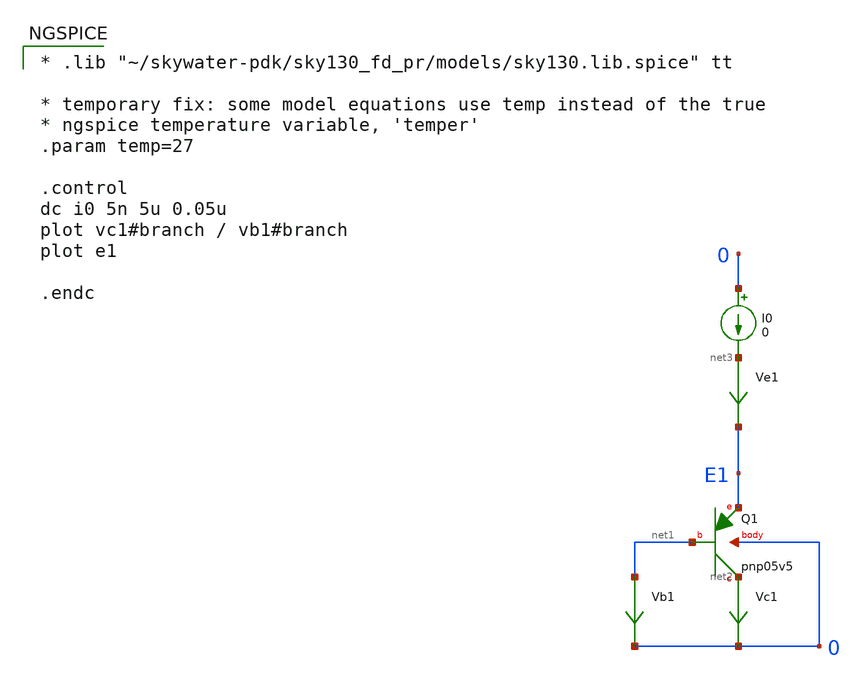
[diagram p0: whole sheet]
** sch_path: sky130_tests/test_bipolar.sch
* Copyright 2020 Stefan Frederik Schippers
* Licensed under the Apache License, Version 2.0 (the "License");
* you may not use this file except in compliance with the License.
* You may obtain a copy of the License at
* https://www.apache.org/licenses/LICENSE-2.0
* Unless required by applicable law or agreed to in writing, software
* distributed under the License is distributed on an "AS IS" BASIS,
* WITHOUT WARRANTIES OR CONDITIONS OF ANY KIND, either express or implied.
* See the License for the specific language governing permissions and
* limitations under the License.
**.subckt test_bipolar
XQ1 net2 net1 E1 0 sky130_fd_pr__pnp_05v5_W0p68L0p68
Vc1 net2 0 0
.save i(vc1)
Vb1 net1 0 0
.save i(vb1)
I0 0 net3 0
Ve1 net3 E1 0
.save i(ve1)
**** begin user architecture code

* .lib "~/skywater-pdk/sky130_fd_pr/models/sky130.lib.spice" tt

* temporary fix: some model equations use temp instead of the true
* ngspice temperature variable, 'temper'
.param temp=27

.control
dc i0 5n 5u 0.05u
plot vc1#branch / vb1#branch
plot e1

.endc


**** end user architecture code
**.ends
**** begin user architecture code

.include   ~/skywater-pdk/sky130_fd_pr_ngspice/cells/nfet_01v8/sky130_fd_pr__nfet_01v8__tt.corner.spice
.include ~/skywater-pdk/sky130_fd_pr_ngspice/cells/nfet_01v8_lvt/sky130_fd_pr__nfet_01v8_lvt__tt.corner.spice
.include ~/skywater-pdk/sky130_fd_pr_ngspice/cells/pfet_01v8/sky130_fd_pr__pfet_01v8__tt.corner.spice
.include ~/skywater-pdk/sky130_fd_pr_ngspice/cells/nfet_03v3_nvt/sky130_fd_pr__nfet_03v3_nvt__tt.corner.spice
.include ~/skywater-pdk/sky130_fd_pr_ngspice/cells/nfet_05v0_nvt/sky130_fd_pr__nfet_05v0_nvt__tt.corner.spice
.include ~/skywater-pdk/sky130_fd_pr_ngspice/cells/esd_nfet_01v8/sky130_fd_pr__esd_nfet_01v8__tt.corner.spice
.include ~/skywater-pdk/sky130_fd_pr_ngspice/cells/pfet_01v8_lvt/sky130_fd_pr__pfet_01v8_lvt__tt.corner.spice
.include ~/skywater-pdk/sky130_fd_pr_ngspice/cells/pfet_01v8_hvt/sky130_fd_pr__pfet_01v8_hvt__tt.corner.spice
.include ~/skywater-pdk/sky130_fd_pr_ngspice/cells/esd_pfet_g5v0d10v5/sky130_fd_pr__esd_pfet_g5v0d10v5__tt.corner.spice
.include ~/skywater-pdk/sky130_fd_pr_ngspice/cells/pfet_g5v0d10v5/sky130_fd_pr__pfet_g5v0d10v5__tt.corner.spice
.include ~/skywater-pdk/sky130_fd_pr_ngspice/cells/pfet_g5v0d16v0/sky130_fd_pr__pfet_g5v0d16v0__tt.corner.spice
.include ~/skywater-pdk/sky130_fd_pr_ngspice/cells/nfet_g5v0d10v5/sky130_fd_pr__nfet_g5v0d10v5__tt.corner.spice
.include ~/skywater-pdk/sky130_fd_pr_ngspice/cells/nfet_g5v0d16v0/sky130_fd_pr__nfet_g5v0d16v0__tt_discrete.corner.spice
.include ~/skywater-pdk/sky130_fd_pr_ngspice/cells/esd_nfet_g5v0d10v5/sky130_fd_pr__esd_nfet_g5v0d10v5__tt.corner.spice
.include ~/skywater-pdk/sky130_fd_pr_ngspice/models/corners/tt/nonfet.spice
* Mismatch parameters
.include ~/skywater-pdk/sky130_fd_pr_ngspice/cells/nfet_01v8/sky130_fd_pr__nfet_01v8__mismatch.corner.spice
.include ~/skywater-pdk/sky130_fd_pr_ngspice/cells/pfet_01v8/sky130_fd_pr__pfet_01v8__mismatch.corner.spice
.include ~/skywater-pdk/sky130_fd_pr_ngspice/cells/nfet_01v8_lvt/sky130_fd_pr__nfet_01v8_lvt__mismatch.corner.spice
.include ~/skywater-pdk/sky130_fd_pr_ngspice/cells/pfet_01v8_lvt/sky130_fd_pr__pfet_01v8_lvt__mismatch.corner.spice
.include ~/skywater-pdk/sky130_fd_pr_ngspice/cells/pfet_01v8_hvt/sky130_fd_pr__pfet_01v8_hvt__mismatch.corner.spice
.include ~/skywater-pdk/sky130_fd_pr_ngspice/cells/nfet_g5v0d10v5/sky130_fd_pr__nfet_g5v0d10v5__mismatch.corner.spice
.include ~/skywater-pdk/sky130_fd_pr_ngspice/cells/pfet_g5v0d10v5/sky130_fd_pr__pfet_g5v0d10v5__mismatch.corner.spice
.include ~/skywater-pdk/sky130_fd_pr_ngspice/cells/nfet_05v0_nvt/sky130_fd_pr__nfet_05v0_nvt__mismatch.corner.spice
.include ~/skywater-pdk/sky130_fd_pr_ngspice/cells/nfet_03v3_nvt/sky130_fd_pr__nfet_03v3_nvt__mismatch.corner.spice
* Resistor/Capacitor
.include ~/skywater-pdk/sky130_fd_pr_ngspice/models/r+c/res_typical__cap_typical.spice
.include ~/skywater-pdk/sky130_fd_pr_ngspice/models/r+c/res_typical__cap_typical__lin.spice
* Special cells
.include ~/skywater-pdk/sky130_fd_pr_ngspice/models/corners/tt/specialized_cells.spice
* All models
.include ~/skywater-pdk/sky130_fd_pr_ngspice/models/all.spice
* Corner
.include ~/skywater-pdk/sky130_fd_pr_ngspice/models/corners/tt/rf.spice


**** end user architecture code
.end
